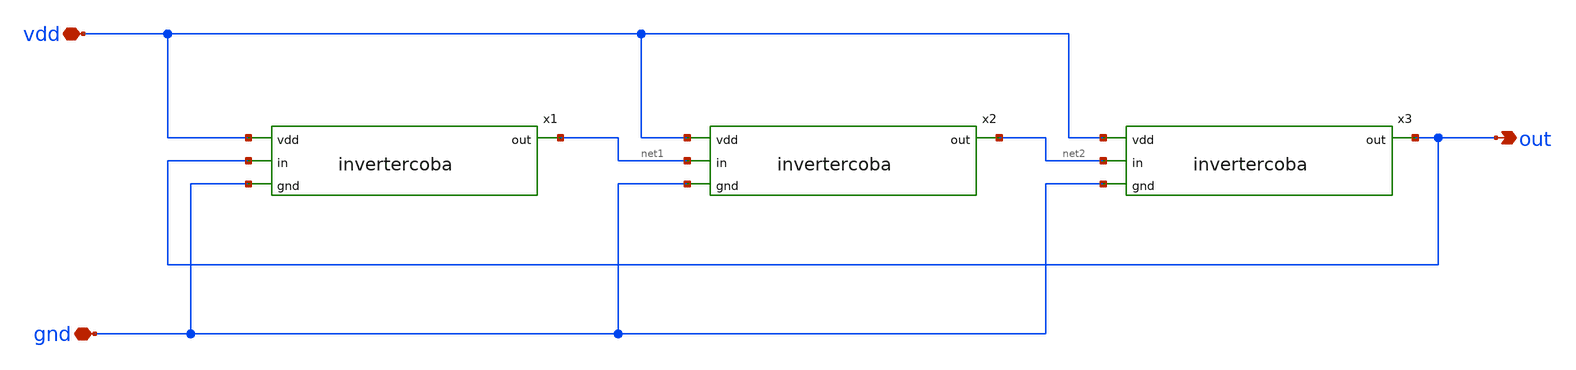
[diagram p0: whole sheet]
** sch_path: ringosi/ringosi.sch
**.subckt ringosi vdd gnd out
*.iopin vdd
*.iopin gnd
*.opin out
x1 vdd out net1 gnd invertercoba
x2 vdd net1 net2 gnd invertercoba
x3 vdd net2 out gnd invertercoba
**.ends
.end
